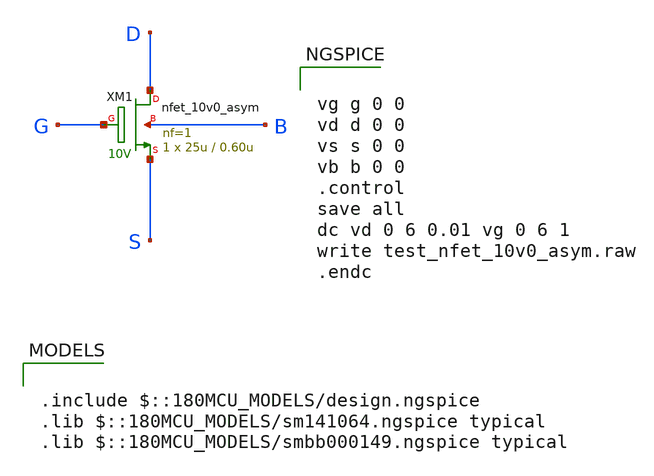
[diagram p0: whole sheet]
** sch_path: gf180mcuD/xschem_libs/gf180mcu_tests/test_nfet_10v0_asym/schematic/test_nfet_10v0_asym.sch
* Copyright 2022 GlobalFoundries PDK Authors
* Licensed under the Apache License, Version 2.0 (the "License");
* you may not use this file except in compliance with the License.
* You may obtain a copy of the License at
* https://www.apache.org/licenses/LICENSE-2.0
* Unless required by applicable law or agreed to in writing, software
* distributed under the License is distributed on an "AS IS" BASIS,
* WITHOUT WARRANTIES OR CONDITIONS OF ANY KIND, either express or implied.
* See the License for the specific language governing permissions and
* limitations under the License.
**.subckt test_nfet_10v0_asym
XM1 D G S B nfet_10v0_asym L=0.60u W=25u nf=1 ad='W * 1.48u' as='W * 0.48u' pd='2 * (W + 1.48u)' ps='2 * (W + 0.48u)'
+ nrd=0 nrs=0 sa=0 sb=0 sd=0 m=1
**** begin user architecture code

.include $::180MCU_MODELS/design.ngspice
.lib $::180MCU_MODELS/sm141064.ngspice typical
.lib $::180MCU_MODELS/smbb000149.ngspice typical



vg g 0 0
vd d 0 0
vs s 0 0
vb b 0 0
.control
save all
dc vd 0 6 0.01 vg 0 6 1
write test_nfet_10v0_asym.raw
.endc


**** end user architecture code
**.ends
.end
